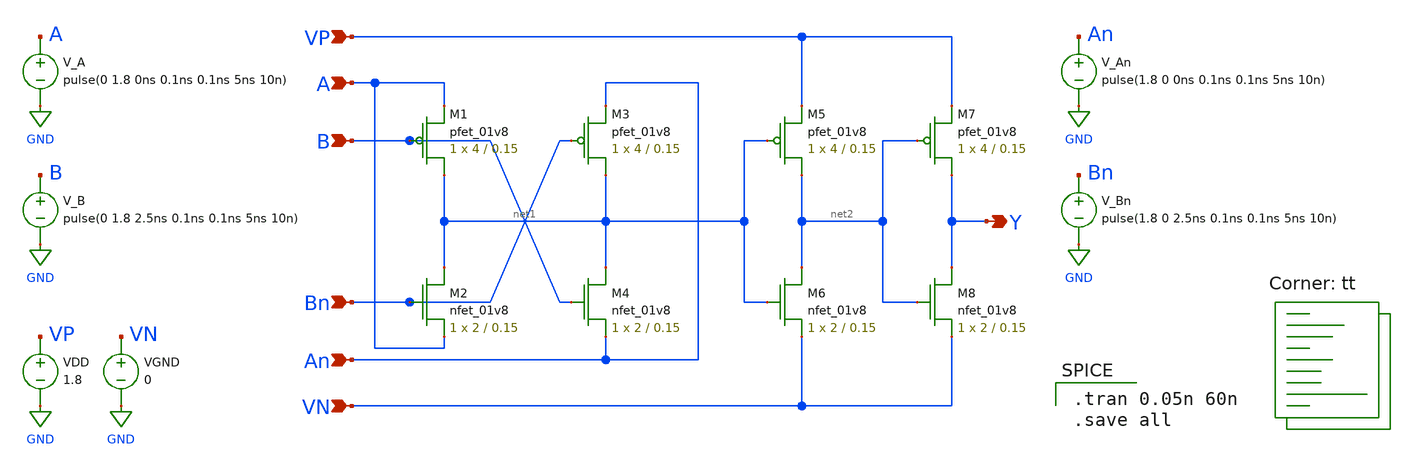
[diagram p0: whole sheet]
** sch_path: Mixed-Signal TRNG/xschem/xor.sch
**.subckt xor B Bn A An Y VP VN
*.ipin B
*.ipin Bn
*.ipin A
*.ipin An
*.opin Y
*.ipin VP
*.ipin VN
XM3 net1 Bn An VP sky130_fd_pr__pfet_01v8 L=0.15 W=4 nf=1 ad='int((nf+1)/2) * W/nf * 0.29' as='int((nf+2)/2) * W/nf * 0.29'
+ pd='2*int((nf+1)/2) * (W/nf + 0.29)' ps='2*int((nf+2)/2) * (W/nf + 0.29)' nrd='0.29 / W' nrs='0.29 / W'
+ sa=0 sb=0 sd=0 mult=1 m=1
XM4 net1 B An VN sky130_fd_pr__nfet_01v8 L=0.15 W=2 nf=1 ad='int((nf+1)/2) * W/nf * 0.29' as='int((nf+2)/2) * W/nf * 0.29'
+ pd='2*int((nf+1)/2) * (W/nf + 0.29)' ps='2*int((nf+2)/2) * (W/nf + 0.29)' nrd='0.29 / W' nrs='0.29 / W'
+ sa=0 sb=0 sd=0 mult=1 m=1
XM5 net2 net1 VP VP sky130_fd_pr__pfet_01v8 L=0.15 W=4 nf=1 ad='int((nf+1)/2) * W/nf * 0.29' as='int((nf+2)/2) * W/nf * 0.29'
+ pd='2*int((nf+1)/2) * (W/nf + 0.29)' ps='2*int((nf+2)/2) * (W/nf + 0.29)' nrd='0.29 / W' nrs='0.29 / W'
+ sa=0 sb=0 sd=0 mult=1 m=1
XM6 net2 net1 VN VN sky130_fd_pr__nfet_01v8 L=0.15 W=2 nf=1 ad='int((nf+1)/2) * W/nf * 0.29' as='int((nf+2)/2) * W/nf * 0.29'
+ pd='2*int((nf+1)/2) * (W/nf + 0.29)' ps='2*int((nf+2)/2) * (W/nf + 0.29)' nrd='0.29 / W' nrs='0.29 / W'
+ sa=0 sb=0 sd=0 mult=1 m=1
XM1 net1 B A VP sky130_fd_pr__pfet_01v8 L=0.15 W=4 nf=1 ad='int((nf+1)/2) * W/nf * 0.29' as='int((nf+2)/2) * W/nf * 0.29'
+ pd='2*int((nf+1)/2) * (W/nf + 0.29)' ps='2*int((nf+2)/2) * (W/nf + 0.29)' nrd='0.29 / W' nrs='0.29 / W'
+ sa=0 sb=0 sd=0 mult=1 m=1
XM2 net1 Bn A VN sky130_fd_pr__nfet_01v8 L=0.15 W=2 nf=1 ad='int((nf+1)/2) * W/nf * 0.29' as='int((nf+2)/2) * W/nf * 0.29'
+ pd='2*int((nf+1)/2) * (W/nf + 0.29)' ps='2*int((nf+2)/2) * (W/nf + 0.29)' nrd='0.29 / W' nrs='0.29 / W'
+ sa=0 sb=0 sd=0 mult=1 m=1
VDD VP GND 1.8
VGND VN GND 0
V_A A GND pulse(0 1.8 0ns 0.1ns 0.1ns 5ns 10n)
V_B B GND pulse(0 1.8 2.5ns 0.1ns 0.1ns 5ns 10n)
V_An An GND pulse(1.8 0 0ns 0.1ns 0.1ns 5ns 10n)
V_Bn Bn GND pulse(1.8 0 2.5ns 0.1ns 0.1ns 5ns 10n)
XM7 Y net2 VP VP sky130_fd_pr__pfet_01v8 L=0.15 W=4 nf=1 ad='int((nf+1)/2) * W/nf * 0.29' as='int((nf+2)/2) * W/nf * 0.29'
+ pd='2*int((nf+1)/2) * (W/nf + 0.29)' ps='2*int((nf+2)/2) * (W/nf + 0.29)' nrd='0.29 / W' nrs='0.29 / W'
+ sa=0 sb=0 sd=0 mult=1 m=1
XM8 Y net2 VN VN sky130_fd_pr__nfet_01v8 L=0.15 W=2 nf=1 ad='int((nf+1)/2) * W/nf * 0.29' as='int((nf+2)/2) * W/nf * 0.29'
+ pd='2*int((nf+1)/2) * (W/nf + 0.29)' ps='2*int((nf+2)/2) * (W/nf + 0.29)' nrd='0.29 / W' nrs='0.29 / W'
+ sa=0 sb=0 sd=0 mult=1 m=1
**** begin user architecture code

.tran 0.05n 60n
.save all

.lib $::SKYWATER_MODELS/sky130.lib.spice tt
**** end user architecture code
**.ends
.GLOBAL GND
.end
